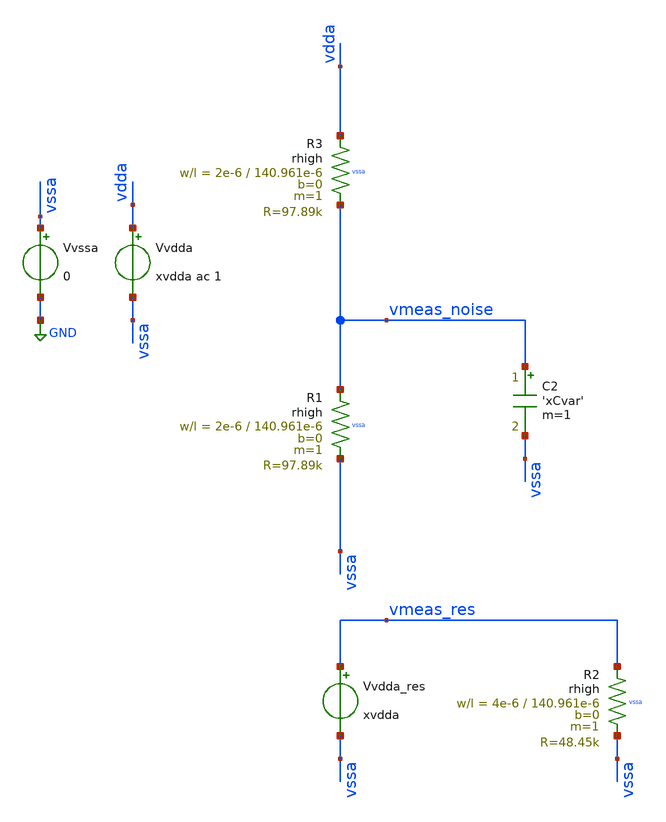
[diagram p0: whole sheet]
** sch_path: ihp_rhigh_thermal_noise_modelling/tb_res_noise.sch
**.subckt tb_res_noise
Vvssa vssa GND 0
Vvdda vdda vssa xvdda ac 1
C2 vmeas_noise vssa 'xCvar' m=1
Vvdda_res vmeas_res vssa xvdda
XR3 vdda vmeas_noise vssa rhigh w=2e-6 l=140.961e-6 m=1 b=0 mm_ok=1
XR1 vmeas_noise vssa vssa rhigh w=2e-6 l=140.961e-6 m=1 b=0 mm_ok=1
XR2 vmeas_res vssa vssa rhigh w=4e-6 l=140.961e-6 m=1 b=0 mm_ok=1
**** begin user architecture code

** opencircuitdesign pdks install
.lib /home/slice/pdk/iHP/IHP-Open-PDK/ihp-sg13g2/libs.tech/ngspice/models/cornerRES.lib res_typ
.lib /home/slice/pdk/iHP/IHP-Open-PDK/ihp-sg13g2/libs.tech/ngspice/models/cornerMOSlv.lib mos_tt
.lib /home/slice/pdk/iHP/IHP-Open-PDK/ihp-sg13g2/libs.tech/ngspice/models/cornerMOShv.lib mos_tt
.include /home/slice/pdk/iHP/IHP-Open-PDK/ihp-sg13g2/libs.ref/sg13g2_stdcell/spice/sg13g2_stdcell.spice

* Parameters

.param xvdda = 1
.param xRvar = 10k
.csparam xRvar_var = 'xRvar'
.param xCvar = 1p
.csparam xCvar_var = 'xCvar'
.param xtsim = 5u
.csparam xtsim_var = 'xtsim'

.temp 27


* vlogA instantiation
.model ideal_sw ideal_sw

.include tb_res_noise.save

* must use .save all for ac noise analysys
  .save all

  .control

  pre_osdi ideal_sw.osdi

 * commercial temperature range
 set xTj = ( 0 10 20 30 40 50 60 70 )
 * industrial temperature range
 *set xTj = ( -40 -30 -20 -10 0 10 20 30 40 50 60 70 85 )
 * military temperature range
 *set xTj = ( -55 -40 -30 -20 -10 0 10 20 30 40 50 60 70 80 90 100 110 125 )
 * automotive temperature range
 *set xTj = ( -40 -30 -20 -10 0 10 20 30 40 50 60 70 80 90 100 110 120 130 140 150 )
 *set xTj = ( 27 )

  foreach xTj_var $xTj

  let Tj_meas = $xTj_var

  echo temperature is "$&Tj_meas"

  set temp = $xTj_var

** 1. TRAN ANALYSIS **

  tran 1n $&xtsim_var
  *set filetype=ascii
  remzerovec
  write tb_res_noise.raw

 ** 2. TRAN MEASURES **

  meas tran vmeas_avg AVG vmeas_res
  meas tran imeas_avg AVG i(Vvdda_res)
  let rmeas = (vmeas_avg/imeas_avg)*-1
  echo --
  echo "$&Tj_meas" >> res_measures_T.txt
  echo "$&rmeas"
  echo "$&rmeas" >> res_measures_typ.txt
 echo --

** 3. AC NOISE ANALYSIS **

  let xfmax = 1G

  noise v(vmeas_noise) Vvdda dec 10 10 $&xfmax 1
  print v(onoise_total)
  setplot noise1
  set filetype=binary
  remzerovec
  write tb_res_noise_density.raw
  let vnoise_op_int = sqrt(integ(onoise_spectrum*onoise_spectrum))

  let freq_density1 = 1k
  let freq_density2 = 10k
  let freq_density3 = 100k

  let nn = 0
  while frequency[nn] < $&freq_density1
  let nn = nn + 1
  end
  * define vectors of frequncies and values just above and below
  * selected frequeny
  let fnn = frequency[nn]
  let nn1 = nn + 1
  let fnn1 = frequency[nn1]
  let snn = onoise_spectrum[nn]
  let snn1 = onoise_spectrum[nn1]
  *print vector values
  echo --
  echo nn = "$&nn"  freq_density1 = "$&fnn"  noise_density1 = "$&snn"
  echo nn1 = "$&nn1"  freq_density1+ = "$&fnn1"  noise_density1+ = "$&snn1"
  *linear interpolation for exact frequency
  let newsnn = snn1 + (snn - snn1)/(fnn - fnn1)*($&freq_density1 - fnn1)
  echo  freq_density1 = "$&freq_density1"  noise_density1_interp = "$&newsnn"
  echo "$&newsnn" >> noise_ipr_1k.txt
  echo --

  let nn = 0
  while frequency[nn] < $&freq_density2
  let nn = nn + 1
  end
  * define vectors of frequncies and values just above and below
  * selected frequeny
  let fnn = frequency[nn]
  let nn1 = nn + 1
  let fnn1 = frequency[nn1]
  let snn = onoise_spectrum[nn]
  let snn1 = onoise_spectrum[nn1]
  *print vector values
  echo --
  echo nn = "$&nn"  freq_density2 = "$&fnn"  noise_density2 = "$&snn"
  echo nn1 = "$&nn1"  freq_density2+ = "$&fnn1"  noise_density2+ = "$&snn1"
  *linear interpolation for exact frequency
  let newsnn = snn1 + (snn - snn1)/(fnn - fnn1)*($&freq_density2 - fnn1)
  echo  freq_density2 = "$&freq_density2"  noise_density2_interp = "$&newsnn"
  echo "$&newsnn" >> noise_ipr_10k.txt
  echo --

  let nn = 0
  while frequency[nn] < $&freq_density3
  let nn = nn + 1
  end
  * define vectors of frequncies and values just above and below
  * selected frequeny
  let fnn = frequency[nn]
  let nn1 = nn + 1
  let fnn1 = frequency[nn1]
  let snn = onoise_spectrum[nn]
  let snn1 = onoise_spectrum[nn1]
  *print vector values
  echo --
  echo nn = "$&nn"  freq_density3 = "$&fnn"  noise_density3 = "$&snn"
  echo nn1 = "$&nn1"  freq_density3+ = "$&fnn1"  noise_density3+ = "$&snn1"
  *linear interpolation for exact frequency
  let newsnn = snn1 + (snn - snn1)/(fnn - fnn1)*($&freq_density3 - fnn1)
  echo  freq_density3 = "$&freq_density3"  noise_density1_interp = "$&newsnn"
  echo "$&newsnn" >> noise_ipr_100k.txt
  echo --

  setplot noise2
  set filetype=ascii
  remzerovec
  write tb_res_integrated_noise.raw

** 4. AC NOISE MEASURES **

 echo --
 let Vn2 = 4*1.38e-23*($xTj_var+273.15)*($&xRvar_var/2)
 print Vn2
 echo --
 let Vn = sqrt(Vn2)
 print Vn
 echo --
 let BW = 1/(2*3.1416*($&xRvar_var/2)*$&xcvar_var)
 print BW
 echo --
 let ENBW = (3.1416/2)*$&BW
 print ENBW
 echo --
 let Vnrms = sqrt($&Vn2*$&ENBW)
 print Vnrms
 echo --

  end

  setplot
*quit 0
.endc




**** end user architecture code
**.ends
.GLOBAL GND
.end
